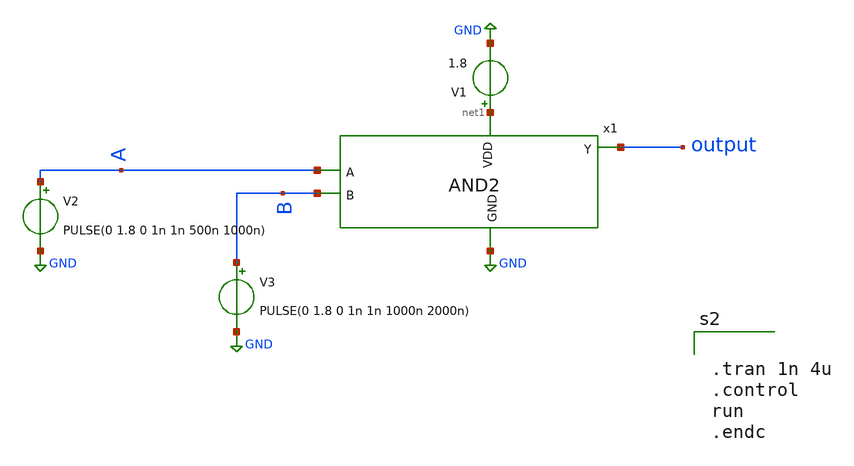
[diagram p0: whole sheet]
** sch_path: ADC/16bit_C2C/MagicAndSpice/EE431_FinalProj/AND2_TB.sch
**.subckt AND2_TB
x1 net1 output A B GND AND2
V1 net1 GND 1.8
V2 A GND PULSE(0 1.8 0 1n 1n 500n 1000n)
V3 B GND PULSE(0 1.8 0 1n 1n 1000n 2000n)
**** begin user architecture code
 .lib $::SKYWATER_MODELS/sky130.lib.spice tt


.tran 1n 4u
.control
run
.endc

**** end user architecture code
**.ends
.GLOBAL GND
.end
